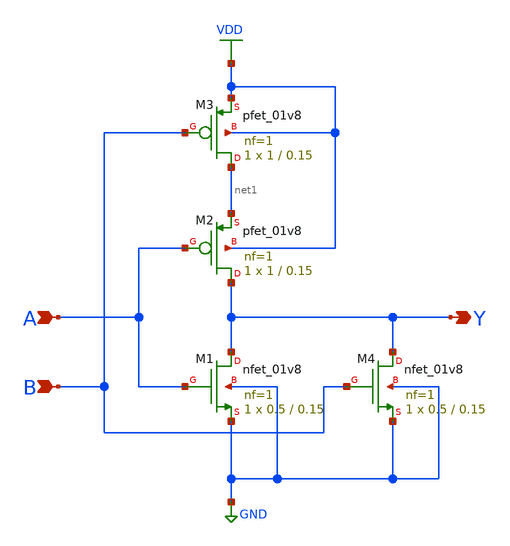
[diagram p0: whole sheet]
** sch_path: xschem/nor.sch
**.subckt nor A Y B
*.ipin A
*.opin Y
*.ipin B
XM1 Y A GND GND sky130_fd_pr__nfet_01v8 L=0.15 W=0.5 nf=1 ad='int((nf+1)/2) * W/nf * 0.29' as='int((nf+2)/2) * W/nf * 0.29'
+ pd='2*int((nf+1)/2) * (W/nf + 0.29)' ps='2*int((nf+2)/2) * (W/nf + 0.29)' nrd='0.29 / W' nrs='0.29 / W'
+ sa=0 sb=0 sd=0 mult=1 m=1
XM2 Y A net1 VDD sky130_fd_pr__pfet_01v8 L=0.15 W=1 nf=1 ad='int((nf+1)/2) * W/nf * 0.29' as='int((nf+2)/2) * W/nf * 0.29'
+ pd='2*int((nf+1)/2) * (W/nf + 0.29)' ps='2*int((nf+2)/2) * (W/nf + 0.29)' nrd='0.29 / W' nrs='0.29 / W'
+ sa=0 sb=0 sd=0 mult=1 m=1
XM3 net1 B VDD VDD sky130_fd_pr__pfet_01v8 L=0.15 W=1 nf=1 ad='int((nf+1)/2) * W/nf * 0.29' as='int((nf+2)/2) * W/nf * 0.29'
+ pd='2*int((nf+1)/2) * (W/nf + 0.29)' ps='2*int((nf+2)/2) * (W/nf + 0.29)' nrd='0.29 / W' nrs='0.29 / W'
+ sa=0 sb=0 sd=0 mult=1 m=1
XM4 Y B GND GND sky130_fd_pr__nfet_01v8 L=0.15 W=0.5 nf=1 ad='int((nf+1)/2) * W/nf * 0.29' as='int((nf+2)/2) * W/nf * 0.29'
+ pd='2*int((nf+1)/2) * (W/nf + 0.29)' ps='2*int((nf+2)/2) * (W/nf + 0.29)' nrd='0.29 / W' nrs='0.29 / W'
+ sa=0 sb=0 sd=0 mult=1 m=1
**.ends
.GLOBAL VDD
.GLOBAL GND
.end
